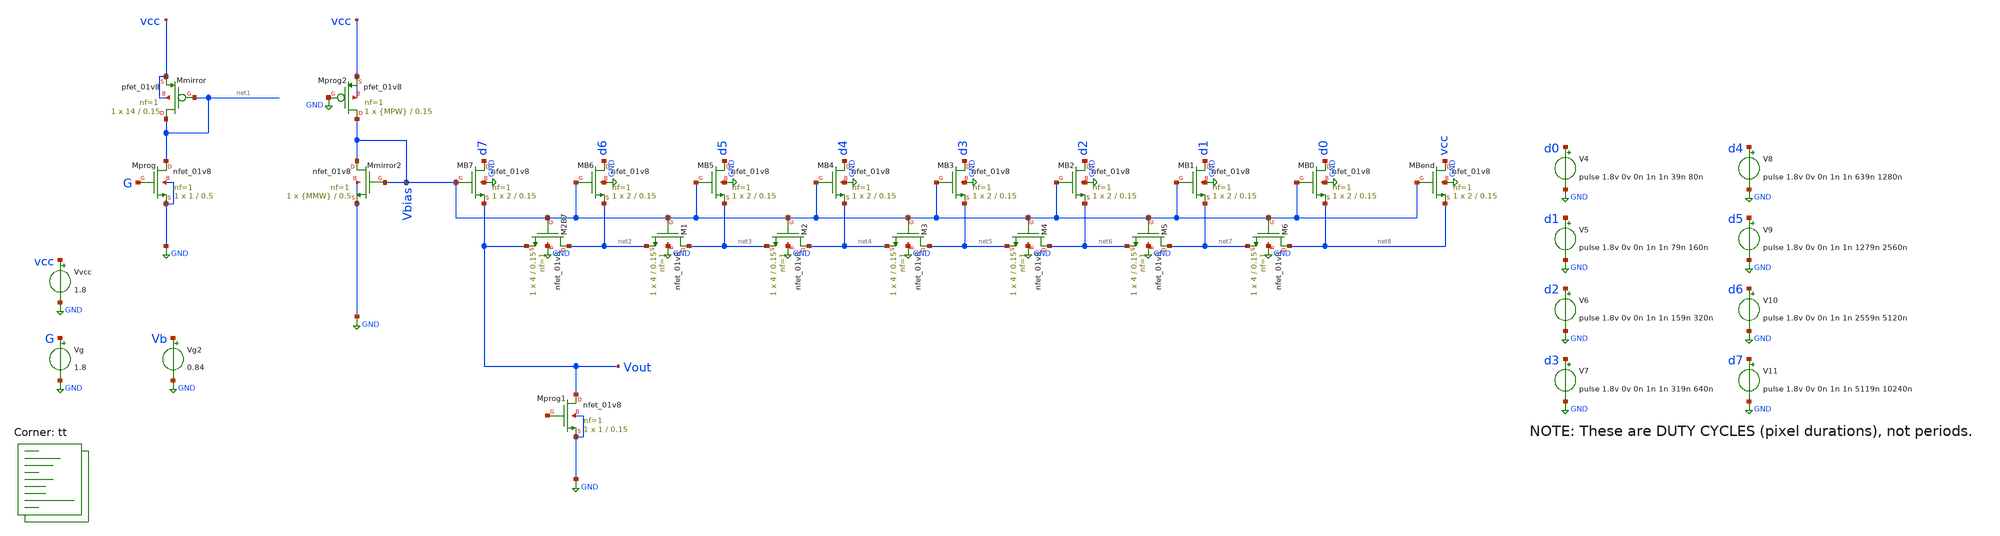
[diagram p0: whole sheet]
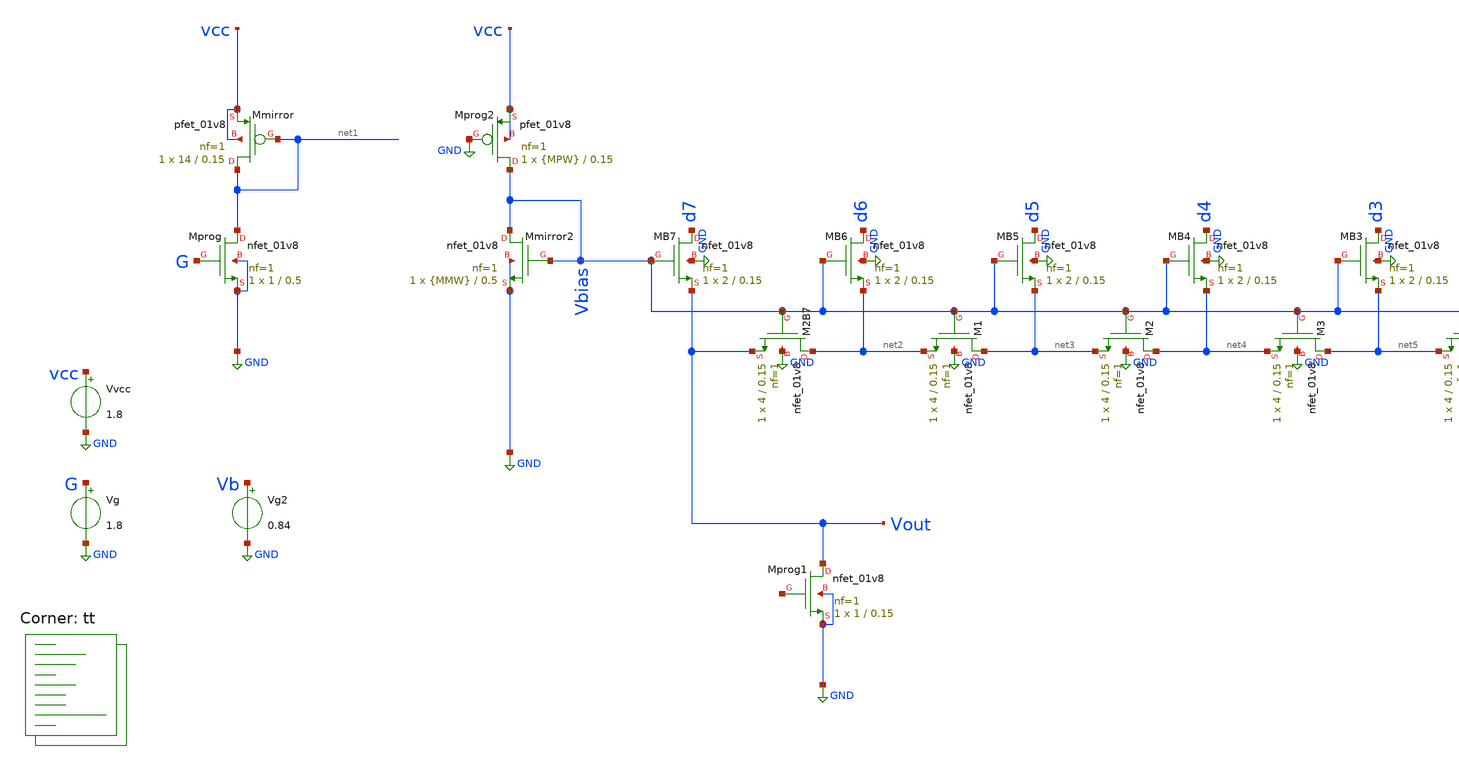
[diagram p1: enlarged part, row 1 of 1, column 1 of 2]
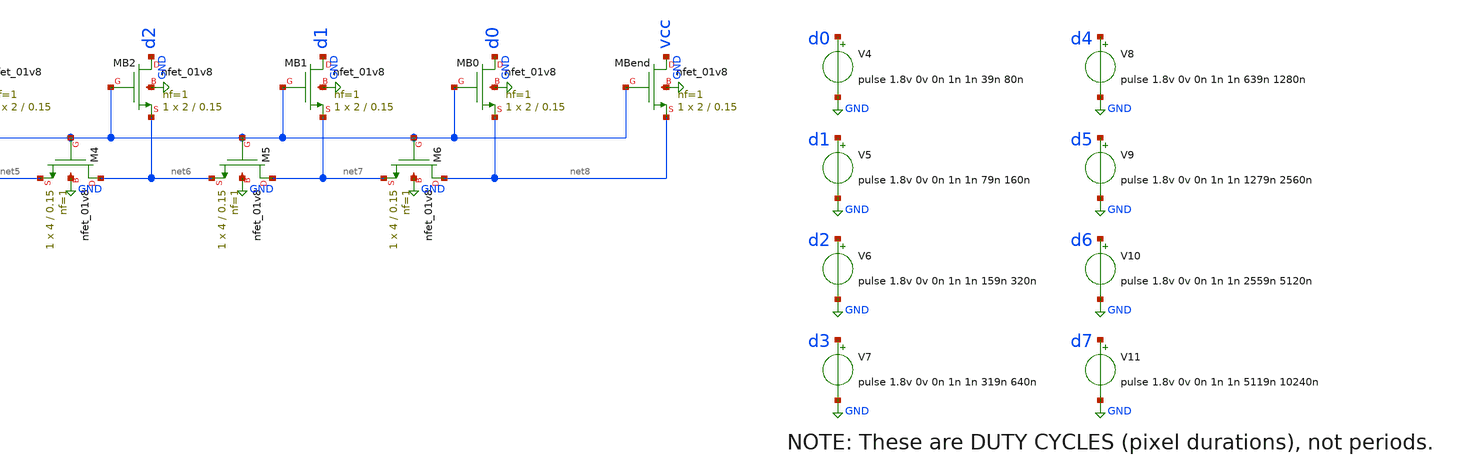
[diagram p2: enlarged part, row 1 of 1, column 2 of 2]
** sch_path: xschem/09-w2w.sch
**.subckt 09-w2w
Vvcc vcc GND 1.8
Vg2 Vb GND 0.84
Vg G GND 1.8
XMprog net1 G GND GND sky130_fd_pr__nfet_01v8 L=0.5 W=1 nf=1 ad='int((nf+1)/2) * W/nf * 0.29' as='int((nf+2)/2) * W/nf * 0.29'
+ pd='2*int((nf+1)/2) * (W/nf + 0.29)' ps='2*int((nf+2)/2) * (W/nf + 0.29)' nrd='0.29 / W' nrs='0.29 / W'
+ sa=0 sb=0 sd=0 mult=1 m=1
XMmirror net1 net1 vcc vcc sky130_fd_pr__pfet_01v8 L=0.15 W=14 nf=1 ad='int((nf+1)/2) * W/nf * 0.29'
+ as='int((nf+2)/2) * W/nf * 0.29' pd='2*int((nf+1)/2) * (W/nf + 0.29)' ps='2*int((nf+2)/2) * (W/nf + 0.29)'
+ nrd='0.29 / W' nrs='0.29 / W' sa=0 sb=0 sd=0 mult=1 m=1
XMprog2 Vbias GND vcc vcc sky130_fd_pr__pfet_01v8 L=0.15 W={MPW} nf=1 ad='int((nf+1)/2) * W/nf * 0.29'
+ as='int((nf+2)/2) * W/nf * 0.29' pd='2*int((nf+1)/2) * (W/nf + 0.29)' ps='2*int((nf+2)/2) * (W/nf + 0.29)'
+ nrd='0.29 / W' nrs='0.29 / W' sa=0 sb=0 sd=0 mult=1 m=1
XMmirror2 Vbias Vbias GND GND sky130_fd_pr__nfet_01v8 L=0.5 W={MMW} nf=1 ad='int((nf+1)/2) * W/nf * 0.29'
+ as='int((nf+2)/2) * W/nf * 0.29' pd='2*int((nf+1)/2) * (W/nf + 0.29)' ps='2*int((nf+2)/2) * (W/nf + 0.29)'
+ nrd='0.29 / W' nrs='0.29 / W' sa=0 sb=0 sd=0 mult=1 m=1
XMB7 d7 Vbias Vout GND sky130_fd_pr__nfet_01v8 L=0.15 W=2 nf=1 ad='int((nf+1)/2) * W/nf * 0.29' as='int((nf+2)/2) * W/nf * 0.29'
+ pd='2*int((nf+1)/2) * (W/nf + 0.29)' ps='2*int((nf+2)/2) * (W/nf + 0.29)' nrd='0.29 / W' nrs='0.29 / W'
+ sa=0 sb=0 sd=0 mult=1 m=1
XM2B7 net2 Vbias Vout GND sky130_fd_pr__nfet_01v8 L=0.15 W=4 nf=1 ad='int((nf+1)/2) * W/nf * 0.29' as='int((nf+2)/2) * W/nf * 0.29'
+ pd='2*int((nf+1)/2) * (W/nf + 0.29)' ps='2*int((nf+2)/2) * (W/nf + 0.29)' nrd='0.29 / W' nrs='0.29 / W'
+ sa=0 sb=0 sd=0 mult=1 m=1
XMB1 d1 Vbias net7 GND sky130_fd_pr__nfet_01v8 L=0.15 W=2 nf=1 ad='int((nf+1)/2) * W/nf * 0.29' as='int((nf+2)/2) * W/nf * 0.29'
+ pd='2*int((nf+1)/2) * (W/nf + 0.29)' ps='2*int((nf+2)/2) * (W/nf + 0.29)' nrd='0.29 / W' nrs='0.29 / W'
+ sa=0 sb=0 sd=0 mult=1 m=1
XM1 net3 Vbias net2 GND sky130_fd_pr__nfet_01v8 L=0.15 W=4 nf=1 ad='int((nf+1)/2) * W/nf * 0.29' as='int((nf+2)/2) * W/nf * 0.29'
+ pd='2*int((nf+1)/2) * (W/nf + 0.29)' ps='2*int((nf+2)/2) * (W/nf + 0.29)' nrd='0.29 / W' nrs='0.29 / W'
+ sa=0 sb=0 sd=0 mult=1 m=1
XMB2 d2 Vbias net6 GND sky130_fd_pr__nfet_01v8 L=0.15 W=2 nf=1 ad='int((nf+1)/2) * W/nf * 0.29' as='int((nf+2)/2) * W/nf * 0.29'
+ pd='2*int((nf+1)/2) * (W/nf + 0.29)' ps='2*int((nf+2)/2) * (W/nf + 0.29)' nrd='0.29 / W' nrs='0.29 / W'
+ sa=0 sb=0 sd=0 mult=1 m=1
XM2 net4 Vbias net3 GND sky130_fd_pr__nfet_01v8 L=0.15 W=4 nf=1 ad='int((nf+1)/2) * W/nf * 0.29' as='int((nf+2)/2) * W/nf * 0.29'
+ pd='2*int((nf+1)/2) * (W/nf + 0.29)' ps='2*int((nf+2)/2) * (W/nf + 0.29)' nrd='0.29 / W' nrs='0.29 / W'
+ sa=0 sb=0 sd=0 mult=1 m=1
XMB3 d3 Vbias net5 GND sky130_fd_pr__nfet_01v8 L=0.15 W=2 nf=1 ad='int((nf+1)/2) * W/nf * 0.29' as='int((nf+2)/2) * W/nf * 0.29'
+ pd='2*int((nf+1)/2) * (W/nf + 0.29)' ps='2*int((nf+2)/2) * (W/nf + 0.29)' nrd='0.29 / W' nrs='0.29 / W'
+ sa=0 sb=0 sd=0 mult=1 m=1
XM3 net5 Vbias net4 GND sky130_fd_pr__nfet_01v8 L=0.15 W=4 nf=1 ad='int((nf+1)/2) * W/nf * 0.29' as='int((nf+2)/2) * W/nf * 0.29'
+ pd='2*int((nf+1)/2) * (W/nf + 0.29)' ps='2*int((nf+2)/2) * (W/nf + 0.29)' nrd='0.29 / W' nrs='0.29 / W'
+ sa=0 sb=0 sd=0 mult=1 m=1
XMB4 d4 Vbias net4 GND sky130_fd_pr__nfet_01v8 L=0.15 W=2 nf=1 ad='int((nf+1)/2) * W/nf * 0.29' as='int((nf+2)/2) * W/nf * 0.29'
+ pd='2*int((nf+1)/2) * (W/nf + 0.29)' ps='2*int((nf+2)/2) * (W/nf + 0.29)' nrd='0.29 / W' nrs='0.29 / W'
+ sa=0 sb=0 sd=0 mult=1 m=1
XM4 net6 Vbias net5 GND sky130_fd_pr__nfet_01v8 L=0.15 W=4 nf=1 ad='int((nf+1)/2) * W/nf * 0.29' as='int((nf+2)/2) * W/nf * 0.29'
+ pd='2*int((nf+1)/2) * (W/nf + 0.29)' ps='2*int((nf+2)/2) * (W/nf + 0.29)' nrd='0.29 / W' nrs='0.29 / W'
+ sa=0 sb=0 sd=0 mult=1 m=1
XMB5 d5 Vbias net3 GND sky130_fd_pr__nfet_01v8 L=0.15 W=2 nf=1 ad='int((nf+1)/2) * W/nf * 0.29' as='int((nf+2)/2) * W/nf * 0.29'
+ pd='2*int((nf+1)/2) * (W/nf + 0.29)' ps='2*int((nf+2)/2) * (W/nf + 0.29)' nrd='0.29 / W' nrs='0.29 / W'
+ sa=0 sb=0 sd=0 mult=1 m=1
XM5 net7 Vbias net6 GND sky130_fd_pr__nfet_01v8 L=0.15 W=4 nf=1 ad='int((nf+1)/2) * W/nf * 0.29' as='int((nf+2)/2) * W/nf * 0.29'
+ pd='2*int((nf+1)/2) * (W/nf + 0.29)' ps='2*int((nf+2)/2) * (W/nf + 0.29)' nrd='0.29 / W' nrs='0.29 / W'
+ sa=0 sb=0 sd=0 mult=1 m=1
XMB6 d6 Vbias net2 GND sky130_fd_pr__nfet_01v8 L=0.15 W=2 nf=1 ad='int((nf+1)/2) * W/nf * 0.29' as='int((nf+2)/2) * W/nf * 0.29'
+ pd='2*int((nf+1)/2) * (W/nf + 0.29)' ps='2*int((nf+2)/2) * (W/nf + 0.29)' nrd='0.29 / W' nrs='0.29 / W'
+ sa=0 sb=0 sd=0 mult=1 m=1
XM6 net8 Vbias net7 GND sky130_fd_pr__nfet_01v8 L=0.15 W=4 nf=1 ad='int((nf+1)/2) * W/nf * 0.29' as='int((nf+2)/2) * W/nf * 0.29'
+ pd='2*int((nf+1)/2) * (W/nf + 0.29)' ps='2*int((nf+2)/2) * (W/nf + 0.29)' nrd='0.29 / W' nrs='0.29 / W'
+ sa=0 sb=0 sd=0 mult=1 m=1
XMB0 d0 Vbias net8 GND sky130_fd_pr__nfet_01v8 L=0.15 W=2 nf=1 ad='int((nf+1)/2) * W/nf * 0.29' as='int((nf+2)/2) * W/nf * 0.29'
+ pd='2*int((nf+1)/2) * (W/nf + 0.29)' ps='2*int((nf+2)/2) * (W/nf + 0.29)' nrd='0.29 / W' nrs='0.29 / W'
+ sa=0 sb=0 sd=0 mult=1 m=1
XMBend vcc Vbias net8 GND sky130_fd_pr__nfet_01v8 L=0.15 W=2 nf=1 ad='int((nf+1)/2) * W/nf * 0.29' as='int((nf+2)/2) * W/nf * 0.29'
+ pd='2*int((nf+1)/2) * (W/nf + 0.29)' ps='2*int((nf+2)/2) * (W/nf + 0.29)' nrd='0.29 / W' nrs='0.29 / W'
+ sa=0 sb=0 sd=0 mult=1 m=1
V4 d0 GND pulse 1.8v 0v 0n 1n 1n 39n 80n
V5 d1 GND pulse 1.8v 0v 0n 1n 1n 79n 160n
V6 d2 GND pulse 1.8v 0v 0n 1n 1n 159n 320n
V7 d3 GND pulse 1.8v 0v 0n 1n 1n 319n 640n
V8 d4 GND pulse 1.8v 0v 0n 1n 1n 639n 1280n
V9 d5 GND pulse 1.8v 0v 0n 1n 1n 1279n 2560n
V10 d6 GND pulse 1.8v 0v 0n 1n 1n 2559n 5120n
V11 d7 GND pulse 1.8v 0v 0n 1n 1n 5119n 10240n
XMprog1 Vout net9 GND GND sky130_fd_pr__nfet_01v8 L=0.15 W=1 nf=1 ad='int((nf+1)/2) * W/nf * 0.29' as='int((nf+2)/2) * W/nf * 0.29'
+ pd='2*int((nf+1)/2) * (W/nf + 0.29)' ps='2*int((nf+2)/2) * (W/nf + 0.29)' nrd='0.29 / W' nrs='0.29 / W'
+ sa=0 sb=0 sd=0 mult=1 m=1
**** begin user architecture code



.param MPW=6
.param MMW=4
.options savecurrents
.control

  save all
  *reset
  *alterparam MPW=6
  *alterparam MMW=4
  tran 1n 12.8u
  write 09.raw Vout

  plot vout

  set appendwrite
  alterparam MPW=5
  alterparam MMW=4
  reset
  tran 1n 12.8u
  write 09.raw Vout

  set appendwrite
  alterparam MPW=4
  alterparam MMW=4
  reset
  tran 1n 12.8u
  write 09.raw Vout

  alterparam MPW=6
  alterparam MMW=3
  reset
  tran 1n 12.8u
  write 09.raw Vout

  set appendwrite
  alterparam MPW=5
  alterparam MMW=3
  reset
  tran 1n 12.8u
  write 09.raw Vout

  set appendwrite
  alterparam MPW=4
  alterparam MMW=3
  reset
  tran 1n 12.8u
  write 09.raw Vout

  alterparam MPW=6
  alterparam MMW=2
  reset
  tran 1n 12.8u
  write 09.raw Vout

  set appendwrite
  alterparam MPW=5
  alterparam MMW=2
  reset
  tran 1n 12.8u
  write 09.raw Vout

  set appendwrite
  alterparam MPW=4
  alterparam MMW=2
  reset
  tran 1n 12.8u
  write 09.raw Vout

.endc



.lib $::SKYWATER_MODELS/sky130.lib.spice tt
**** end user architecture code
**.ends
.GLOBAL GND
.end
